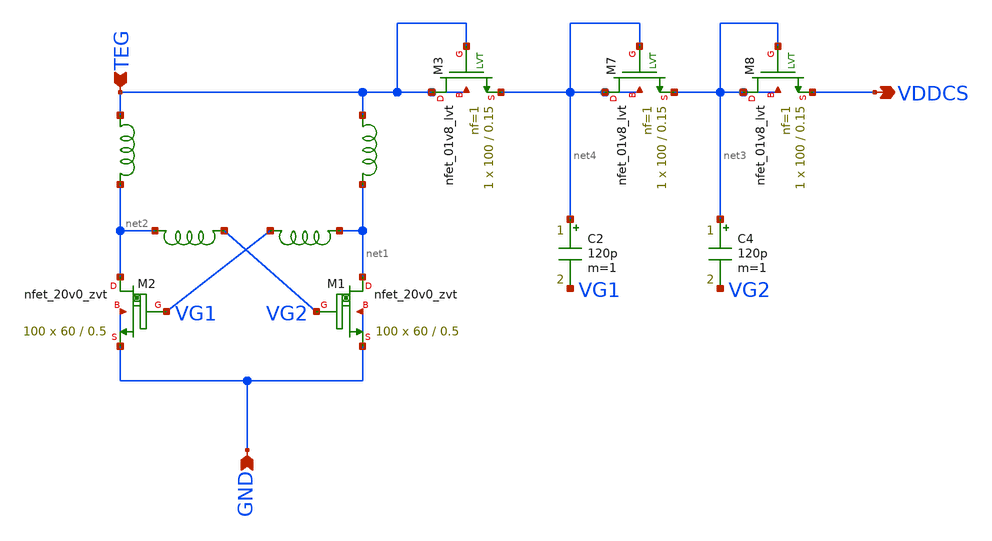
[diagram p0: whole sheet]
** sch_path: design/LELO_SVOD_SKY130A/LELO_COLD_START.sch
**.subckt LELO_COLD_START GND TEG VDDCS
*.ipin GND
*.ipin TEG
*.opin VDDCS
C2 net4 VG1 120p m=1
x1 VG2 net2 1812PS-564_imp
x2 net1 VG1 1812PS-564_imp
C4 net3 VG2 120p m=1
XM1 net1 VG2 GND GND sky130_fd_pr__nfet_20v0_zvt W=60 L=0.5 m=100
XM2 net2 VG1 GND GND sky130_fd_pr__nfet_20v0_zvt W=60 L=0.5 m=100
XM3 TEG TEG net4 TEG sky130_fd_pr__nfet_01v8_lvt L=0.15 W=100 nf=1 ad='int((1 + 1)/2) * 100 / 1 * 0.29'
+ as='int((1 + 2)/2) * 100 / 1 * 0.29' pd='2*int((1 + 1)/2) * (100 / 1 + 0.29)' ps='2*int((1 + 2)/2) * (100 / 1 + 0.29)'
+ nrd='0.29 / 100 ' nrs='0.29 / 100 ' sa=0 sb=0 sd=0 mult=1 m=1
XM7 net4 net4 net3 net4 sky130_fd_pr__nfet_01v8_lvt L=0.15 W=100 nf=1 ad='int((1 + 1)/2) * 100 / 1 * 0.29'
+ as='int((1 + 2)/2) * 100 / 1 * 0.29' pd='2*int((1 + 1)/2) * (100 / 1 + 0.29)' ps='2*int((1 + 2)/2) * (100 / 1 + 0.29)'
+ nrd='0.29 / 100 ' nrs='0.29 / 100 ' sa=0 sb=0 sd=0 mult=1 m=1
XM8 net3 net3 VDDCS net3 sky130_fd_pr__nfet_01v8_lvt L=0.15 W=100 nf=1 ad='int((1 + 1)/2) * 100 / 1 * 0.29'
+ as='int((1 + 2)/2) * 100 / 1 * 0.29' pd='2*int((1 + 1)/2) * (100 / 1 + 0.29)' ps='2*int((1 + 2)/2) * (100 / 1 + 0.29)'
+ nrd='0.29 / 100 ' nrs='0.29 / 100 ' sa=0 sb=0 sd=0 mult=1 m=1
x3 TEG net2 XGL6030-472_sat
x4 TEG net1 XGL6030-472_sat
**.ends

* expanding   symbol:  LELO_SVOD_SKY130A/1812PS-564_imp.sym # of pins=2
** sym_path: design/LELO_SVOD_SKY130A/1812PS-564_imp.sym

.subckt 1812PS-564_imp port1 port2
X1 port1 port2 Model1D R1=70 R2=6.1 C= 7.71p K1=0.000001 K2=115.8 K3= 560u K4=0.000001 K5=0.000001
+ L=0 Is=0 a=0 L_Z0=0 L_EL=0 L_F0=0E6 PkZ=153558.837
.ends 1812PS-564_imp

* expanding   symbol:  LELO_SVOD_SKY130A/XGL6030-472_sat.sym # of pins=2
** sym_path: design/LELO_SVOD_SKY130A/XGL6030-472_sat.sym

.subckt XGL6030-472_sat port1 port2
X1 port1 port2 Model1C R1=5 R2=0.021 C=13.9p K1=0.000001 K2=1.05 K3= 4.7u K4=0.000001 K5=0.000001
+ L=4.5383E-06 Is=18.1418 a=0.725 L_Z0=0 L_EL=0 L_F0=0E6 PkZ=4358.77183
.ends XGL6030-472_sat

.end
